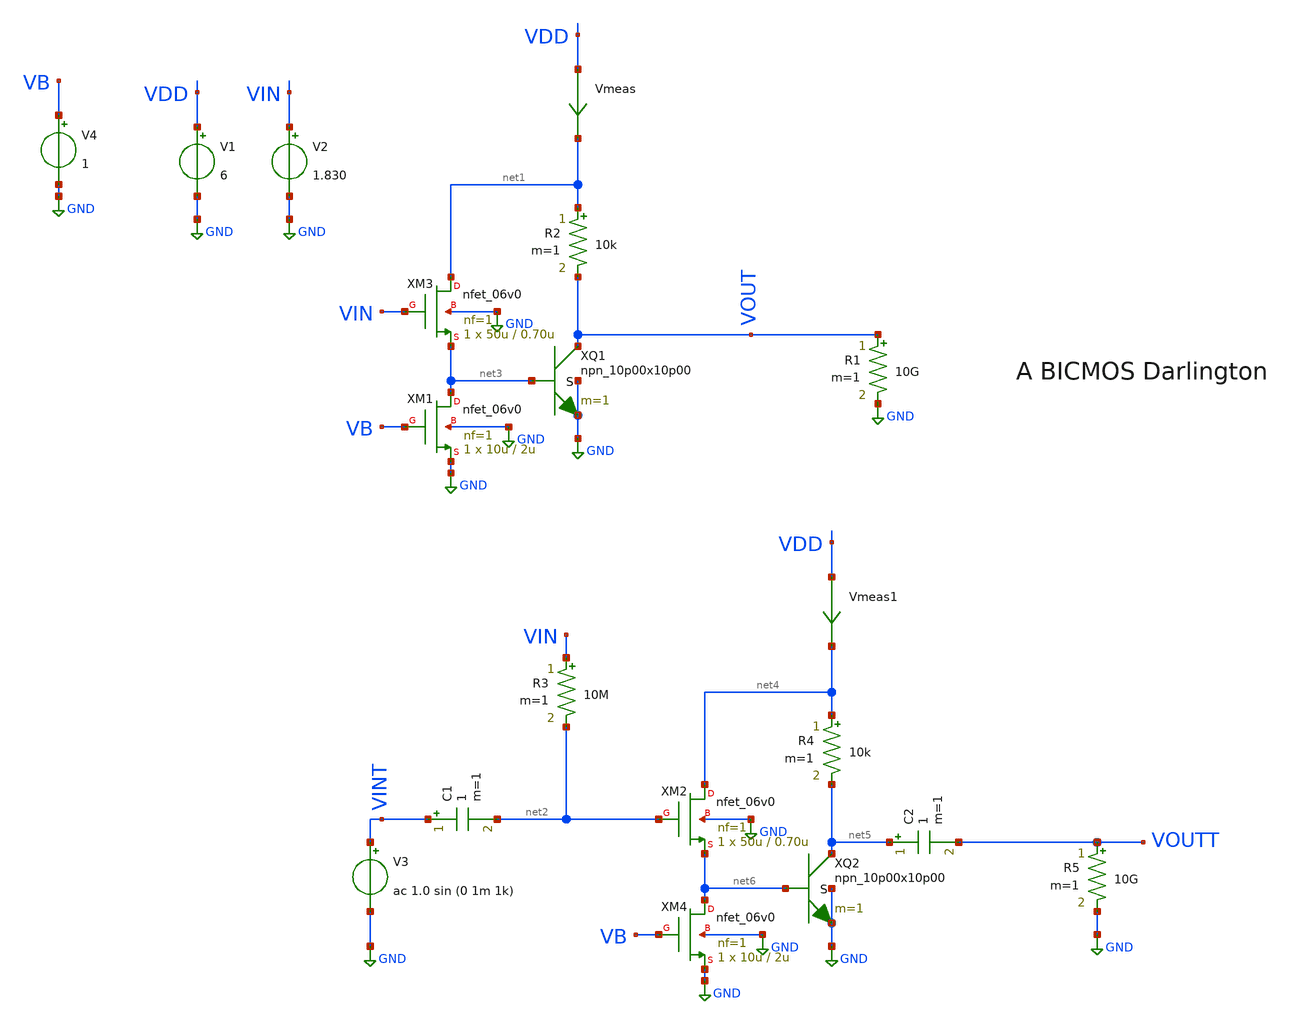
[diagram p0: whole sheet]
** sch_path: basic_circuits/BICMOS_DARLINGTON.sch
**.subckt BICMOS_DARLINGTON
Vmeas VDD net1 0
.save i(vmeas)
V1 VDD GND 6
V2 VIN GND 1.830
V3 VINT GND ac 1.0 sin (0 1m 1k)
R3 VIN net2 10M m=1
R5 VOUTT GND 10G m=1
V4 VB GND 1
R1 VOUT GND 10G m=1
C1 VINT net2 1 m=1
R2 net1 VOUT 10k m=1
XQ1 VOUT net3 GND GND npn_10p00x10p00 m=1
C2 net5 VOUTT 1 m=1
XM3 net1 VIN net3 GND nfet_06v0 L=0.70u W=50u nf=1 ad='int((nf+1)/2) * W/nf * 0.18u' as='int((nf+2)/2) * W/nf * 0.18u'
+ pd='2*int((nf+1)/2) * (W/nf + 0.18u)' ps='2*int((nf+2)/2) * (W/nf + 0.18u)' nrd='0.18u / W' nrs='0.18u / W'
+ sa=0 sb=0 sd=0 m=1
XM1 net3 VB GND GND nfet_06v0 L=2u W=10u nf=1 ad='int((nf+1)/2) * W/nf * 0.18u' as='int((nf+2)/2) * W/nf * 0.18u'
+ pd='2*int((nf+1)/2) * (W/nf + 0.18u)' ps='2*int((nf+2)/2) * (W/nf + 0.18u)' nrd='0.18u / W' nrs='0.18u / W'
+ sa=0 sb=0 sd=0 m=1
Vmeas1 VDD net4 0
.save i(vmeas1)
R4 net4 net5 10k m=1
XQ2 net5 net6 GND GND npn_10p00x10p00 m=1
XM2 net4 net2 net6 GND nfet_06v0 L=0.70u W=50u nf=1 ad='int((nf+1)/2) * W/nf * 0.18u' as='int((nf+2)/2) * W/nf * 0.18u'
+ pd='2*int((nf+1)/2) * (W/nf + 0.18u)' ps='2*int((nf+2)/2) * (W/nf + 0.18u)' nrd='0.18u / W' nrs='0.18u / W'
+ sa=0 sb=0 sd=0 m=1
XM4 net6 VB GND GND nfet_06v0 L=2u W=10u nf=1 ad='int((nf+1)/2) * W/nf * 0.18u' as='int((nf+2)/2) * W/nf * 0.18u'
+ pd='2*int((nf+1)/2) * (W/nf + 0.18u)' ps='2*int((nf+2)/2) * (W/nf + 0.18u)' nrd='0.18u / W' nrs='0.18u / W'
+ sa=0 sb=0 sd=0 m=1
**** begin user architecture code

**************************************************************
**************************************************************
**************************************************************
**************************************************************
**************************************************************
*LIBs*********************************************************
**************************************************************
**************************************************************
**************************************************************
**************************************************************
**************************************************************
.include $::180MCU_MODELS/design.ngspice
*.lib $::180MCU_MODELS/sm141064.ngspice statistical *use statistical if you want global and parameter mismatch
*.lib $::180MCU_MODELS/sm141064.ngspice res_statistical
.lib $::180MCU_MODELS/sm141064.ngspice typical
.lib $::180MCU_MODELS/sm141064.ngspice res_typical
.lib $::180MCU_MODELS/sm141064.ngspice moscap_typical
.lib $::180MCU_MODELS/sm141064.ngspice bjt_typical
.lib $::180MCU_MODELS/sm141064.ngspice diode_typical
.lib $::180MCU_MODELS/sm141064.ngspice mimcap_typical
**************************************************************
**************************************************************
**************************************************************
**************************************************************
**************************************************************
*Corners/montecarlo options***********************************
**************************************************************
**************************************************************
**************************************************************
**************************************************************
**************************************************************
.TEMP 27
.param   sw_stat_global = 1   sw_stat_mism = 1  mc_skew = 3  res_mc_skew = 3  cap_mc_skew = 3
+  fnoicor = 1
**************************************************************
**************************************************************
**************************************************************
**************************************************************
*SIMULATION and Plots*****************************************
**************************************************************
**************************************************************
**************************************************************
**************************************************************
.control
save all
dc V2 0 3.3 0.01
*dc simulation
plot v(VOUT) v(VIN) deriv(v(VOUT))
*ploting VIN VOUT and the voltage gain
plot i(Vmeas)
*ploting the current for curiosity
tran 100ns 2m
*transient simulation
plot (v(VINT)) (v(VOUTT))
*simple plot to exemplify the gain
fft v(VOUTT) v(VINT)
*fast fourier transfor
plot mag(v(VOUTT)) mag(v(VINT))
* analyse the frequency spectrum of the transient waves, to detect distortion
ac dec 20 1 50G
*simple ac simulation
plot v(VOUTT)
*gain in function of the input frequency
.endc

**** end user architecture code
**.ends
.GLOBAL GND
.end
